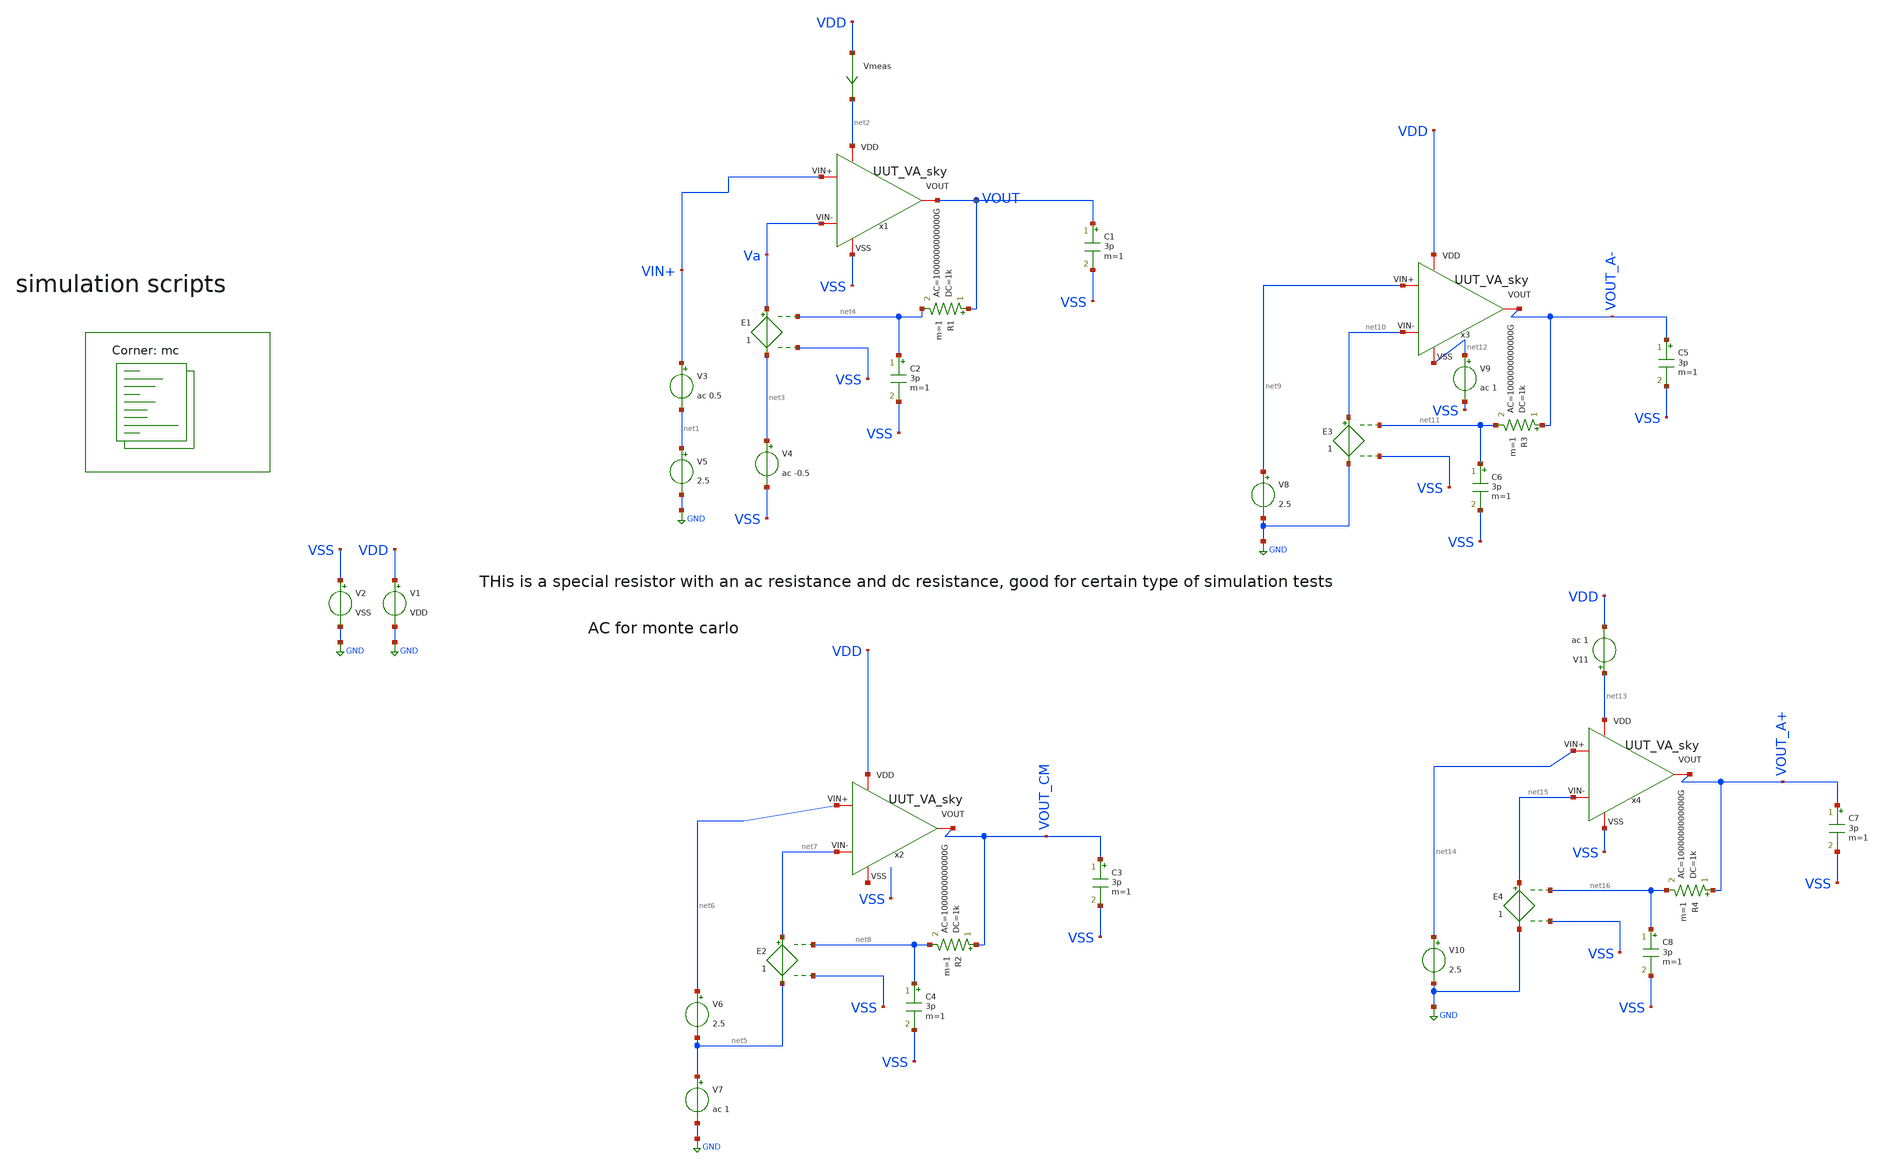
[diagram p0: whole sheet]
** sch_path: Learning/single_ended_amplifiers/Design_and_Analysis_of_Two-Stage_CMOS_Operational_Amplifier_for_Fluorescence_Signal_Processing_sky130_5V/amplifier_design/OTA_mc_ac_tb.sch
**.subckt OTA_mc_ac_tb
V1 VDD GND VDD
V2 VSS GND VSS
Vmeas VDD net2 0
.save i(vmeas)
x1 net2 VSS Va VIN+ VOUT UUT_VA_sky
C1 VOUT VSS 3p m=1
V5 net1 GND 2.5
V3 VIN+ net1 ac 0.5
V4 net3 VSS ac -0.5
E1 Va net3 net4 VSS 1
R1 VOUT net4 1k ac=1000000000000G m=1
C2 net4 VSS 3p m=1
x2 VDD net17 net7 net6 VOUT_CM UUT_VA_sky
C3 VOUT_CM VSS 3p m=1
V6 net6 net5 2.5
V7 net5 GND ac 1
E2 net7 net5 net8 VSS 1
R2 VOUT_CM net8 1k ac=1000000000000G m=1
C4 net8 VSS 3p m=1
x3 VDD net12 net10 net9 VOUT_A- UUT_VA_sky
C5 VOUT_A- VSS 3p m=1
V8 net9 GND 2.5
E3 net10 GND net11 VSS 1
R3 VOUT_A- net11 1k ac=1000000000000G m=1
C6 net11 VSS 3p m=1
V9 net12 VSS ac 1
x4 net13 VSS net15 net14 VOUT_A+ UUT_VA_sky
C7 VOUT_A+ VSS 3p m=1
V10 net14 GND 2.5
E4 net15 GND net16 VSS 1
R4 VOUT_A+ net16 1k ac=1000000000000G m=1
C8 net16 VSS 3p m=1
V11 net13 VDD ac 1
**** begin user architecture code
.lib $::SKYWATER_MODELS/sky130.lib.spice mc

.Temp 27
.param VDD = 5
.param VSS = 0
.param CL = 3p
.param mc_mm_switch = 1


.control

	save all
	ac dec 100 1 10G
	plot db(v(VOUT))
	plot db(v(VOUT_CM))
	plot db(v(VOUT_A-))
	plot db(v(VOUT_A+))
	wrdata mc_ac.csv db(v(VOUT)) phase(v(VOUT)) db(v(VOUT_CM)) db(v(VOUT_A-)) db(v(VOUT_A+))
	noise v(VOUT,VSS) V3 dec 10 1 10G
	setplot noise1

	plot onoise_spectrum inoise_spectrum

.endc


**** end user architecture code
**.ends

* expanding   symbol:  Sky130A/UUT_sky/UUT_VA_sky.sym # of pins=5
** sym_path: my_ip/LIB/Sky130A/UUT_sky/UUT_VA_sky.sym
** sch_path: my_ip/LIB/Sky130A/UUT_sky/UUT_VA_sky.sch
.subckt UUT_VA_sky VDD VSS VIN- VIN+ VOUT
*.iopin VDD
*.iopin VSS
*.iopin VIN-
*.iopin VIN+
*.iopin VOUT
x1 VDD VSS VIN+ VIN- VOUT amplifier
.ends


* expanding   symbol:
*+  Sky130A/Learning/Design_of_Two-Stage_CMOS_Operational_Amplifier_for_Fluorescence_Signal_Processing_5V/amplifier.sym # of pins=5
** sym_path: my_ip/LIB/Sky130A/Learning/Design_of_Two-Stage_CMOS_Operational_Amplifier_for_Fluorescence_Signal_Processing_5V/amplifier.sym
** sch_path: my_ip/LIB/Sky130A/Learning/Design_of_Two-Stage_CMOS_Operational_Amplifier_for_Fluorescence_Signal_Processing_5V/amplifier.sch
.subckt amplifier VDD VSS Vin+ Vin- VOUT
*.iopin VDD
*.iopin VSS
*.iopin Vin+
*.iopin Vin-
*.iopin VOUT
XR2 VSS net2 VSS sky130_fd_pr__res_high_po_0p35 L=20.4 mult=1 m=1
XM7 net1 net1 VSS VSS sky130_fd_pr__nfet_g5v0d10v5 L=3.2 W='1 * 2 ' nf=2 ad='int((nf+1)/2) * W / nf * 0.29'
+ as='int((nf+2)/2) * W / nf * 0.29' pd='2*int((nf+1)/2) * (W / nf + 0.29)' ps='2*int((nf+2)/2) * (W / nf + 0.29)'
+ nrd='0.29 / W ' nrs='0.29 / W ' sa=0 sb=0 sd=0 mult=2 m=2
XM8 net3 net1 net2 VSS sky130_fd_pr__nfet_g5v0d10v5 L=3.2 W='1 * 8 ' nf=8 ad='int((nf+1)/2) * W / nf * 0.29'
+ as='int((nf+2)/2) * W / nf * 0.29' pd='2*int((nf+1)/2) * (W / nf + 0.29)' ps='2*int((nf+2)/2) * (W / nf + 0.29)'
+ nrd='0.29 / W ' nrs='0.29 / W ' sa=0 sb=0 sd=0 mult=2 m=2
XM9 VB1 VB2 net3 VSS sky130_fd_pr__nfet_g5v0d10v5 L=2 W='1 * 2 ' nf=2 ad='int((nf+1)/2) * W / nf * 0.29'
+ as='int((nf+2)/2) * W / nf * 0.29' pd='2*int((nf+1)/2) * (W / nf + 0.29)' ps='2*int((nf+2)/2) * (W / nf + 0.29)'
+ nrd='0.29 / W ' nrs='0.29 / W ' sa=0 sb=0 sd=0 mult=2 m=2
XM10 VB2 VB2 net1 VSS sky130_fd_pr__nfet_g5v0d10v5 L=2 W='1 * 2 ' nf=2 ad='int((nf+1)/2) * W / nf * 0.29'
+ as='int((nf+2)/2) * W / nf * 0.29' pd='2*int((nf+1)/2) * (W / nf + 0.29)' ps='2*int((nf+2)/2) * (W / nf + 0.29)'
+ nrd='0.29 / W ' nrs='0.29 / W ' sa=0 sb=0 sd=0 mult=2 m=2
XM2 net6 Vin- net4 net4 sky130_fd_pr__pfet_g5v0d10v5 L=1 W='4.5 * 2 ' nf=2 ad='int((2 + 1)/2) * 4.5 * 0.29'
+ as='int((2 + 2)/2) * 4.5 * 0.29' pd='2*int((2 + 1)/2) * (4.5 + 0.29)' ps='2*int((2 + 2)/2) * (4.5 + 0.29)'
+ nrd='0.29 / 4.5 / 2 ' nrs='0.29 / 4.5 / 2 ' sa=0 sb=0 sd=0 mult=4 m=4
XM3 net5 Vin+ net4 net4 sky130_fd_pr__pfet_g5v0d10v5 L=1 W='4.5 * 2 ' nf=2 ad='int((2 + 1)/2) * 4.5 * 0.29'
+ as='int((2 + 2)/2) * 4.5 * 0.29' pd='2*int((2 + 1)/2) * (4.5 + 0.29)' ps='2*int((2 + 2)/2) * (4.5 + 0.29)'
+ nrd='0.29 / 4.5 / 2 ' nrs='0.29 / 4.5 / 2 ' sa=0 sb=0 sd=0 mult=4 m=4
XM4 net5 net6 VSS VSS sky130_fd_pr__nfet_g5v0d10v5 L=2 W='1.5 * 2 ' nf=2 ad='int((nf+1)/2) * W / nf * 0.29'
+ as='int((nf+2)/2) * W / nf * 0.29' pd='2*int((nf+1)/2) * (W / nf + 0.29)' ps='2*int((nf+2)/2) * (W / nf + 0.29)'
+ nrd='0.29 / W ' nrs='0.29 / W ' sa=0 sb=0 sd=0 mult=2 m=2
XM11 net6 net6 VSS VSS sky130_fd_pr__nfet_g5v0d10v5 L=2 W='1.5 * 2 ' nf=2 ad='int((nf+1)/2) * W / nf * 0.29'
+ as='int((nf+2)/2) * W / nf * 0.29' pd='2*int((nf+1)/2) * (W / nf + 0.29)' ps='2*int((nf+2)/2) * (W / nf + 0.29)'
+ nrd='0.29 / W ' nrs='0.29 / W ' sa=0 sb=0 sd=0 mult=2 m=2
XM13 VOUT net5 VSS VSS sky130_fd_pr__nfet_g5v0d10v5 L=1 W='4 * 2 ' nf=2 ad='int((nf+1)/2) * W / nf * 0.29'
+ as='int((nf+2)/2) * W / nf * 0.29' pd='2*int((nf+1)/2) * (W / nf + 0.29)' ps='2*int((nf+2)/2) * (W / nf + 0.29)'
+ nrd='0.29 / W ' nrs='0.29 / W ' sa=0 sb=0 sd=0 mult=2 m=2
XM14 net7 VB2 net5 VSS sky130_fd_pr__nfet_g5v0d10v5 L=2 W='1.4 * 1 ' nf=1 ad='int((nf+1)/2) * W / nf * 0.29'
+ as='int((nf+2)/2) * W / nf * 0.29' pd='2*int((nf+1)/2) * (W / nf + 0.29)' ps='2*int((nf+2)/2) * (W / nf + 0.29)'
+ nrd='0.29 / W ' nrs='0.29 / W ' sa=0 sb=0 sd=0 mult=2 m=2
XC1 VOUT net7 sky130_fd_pr__cap_mim_m3_1 W=8 L=8 MF=4 m=4
XM1 VB2 VB1 VDD VDD sky130_fd_pr__pfet_g5v0d10v5 L=2.2 W='1 * 2 ' nf=2 ad='int((2 + 1)/2) * 1 * 0.29'
+ as='int((2 + 2)/2) * 1 * 0.29' pd='2*int((2 + 1)/2) * (1 + 0.29)' ps='2*int((2 + 2)/2) * (1 + 0.29)'
+ nrd='0.29 / 1 / 2 ' nrs='0.29 / 1 / 2 ' sa=0 sb=0 sd=0 mult=2 m=2
XM5 VB1 VB1 VDD VDD sky130_fd_pr__pfet_g5v0d10v5 L=2.2 W='1 * 2 ' nf=2 ad='int((2 + 1)/2) * 1 * 0.29'
+ as='int((2 + 2)/2) * 1 * 0.29' pd='2*int((2 + 1)/2) * (1 + 0.29)' ps='2*int((2 + 2)/2) * (1 + 0.29)'
+ nrd='0.29 / 1 / 2 ' nrs='0.29 / 1 / 2 ' sa=0 sb=0 sd=0 mult=2 m=2
XM6 net4 VB1 VDD VDD sky130_fd_pr__pfet_g5v0d10v5 L=2.2 W='1 * 2 ' nf=2 ad='int((2 + 1)/2) * 1 * 0.29'
+ as='int((2 + 2)/2) * 1 * 0.29' pd='2*int((2 + 1)/2) * (1 + 0.29)' ps='2*int((2 + 2)/2) * (1 + 0.29)'
+ nrd='0.29 / 1 / 2 ' nrs='0.29 / 1 / 2 ' sa=0 sb=0 sd=0 mult=8 m=8
XM12 VOUT VB1 VDD VDD sky130_fd_pr__pfet_g5v0d10v5 L=2.2 W='1 * 2 ' nf=2 ad='int((2 + 1)/2) * 1 * 0.29'
+ as='int((2 + 2)/2) * 1 * 0.29' pd='2*int((2 + 1)/2) * (1 + 0.29)' ps='2*int((2 + 2)/2) * (1 + 0.29)'
+ nrd='0.29 / 1 / 2 ' nrs='0.29 / 1 / 2 ' sa=0 sb=0 sd=0 mult=16 m=16
.ends

.GLOBAL GND
.end
